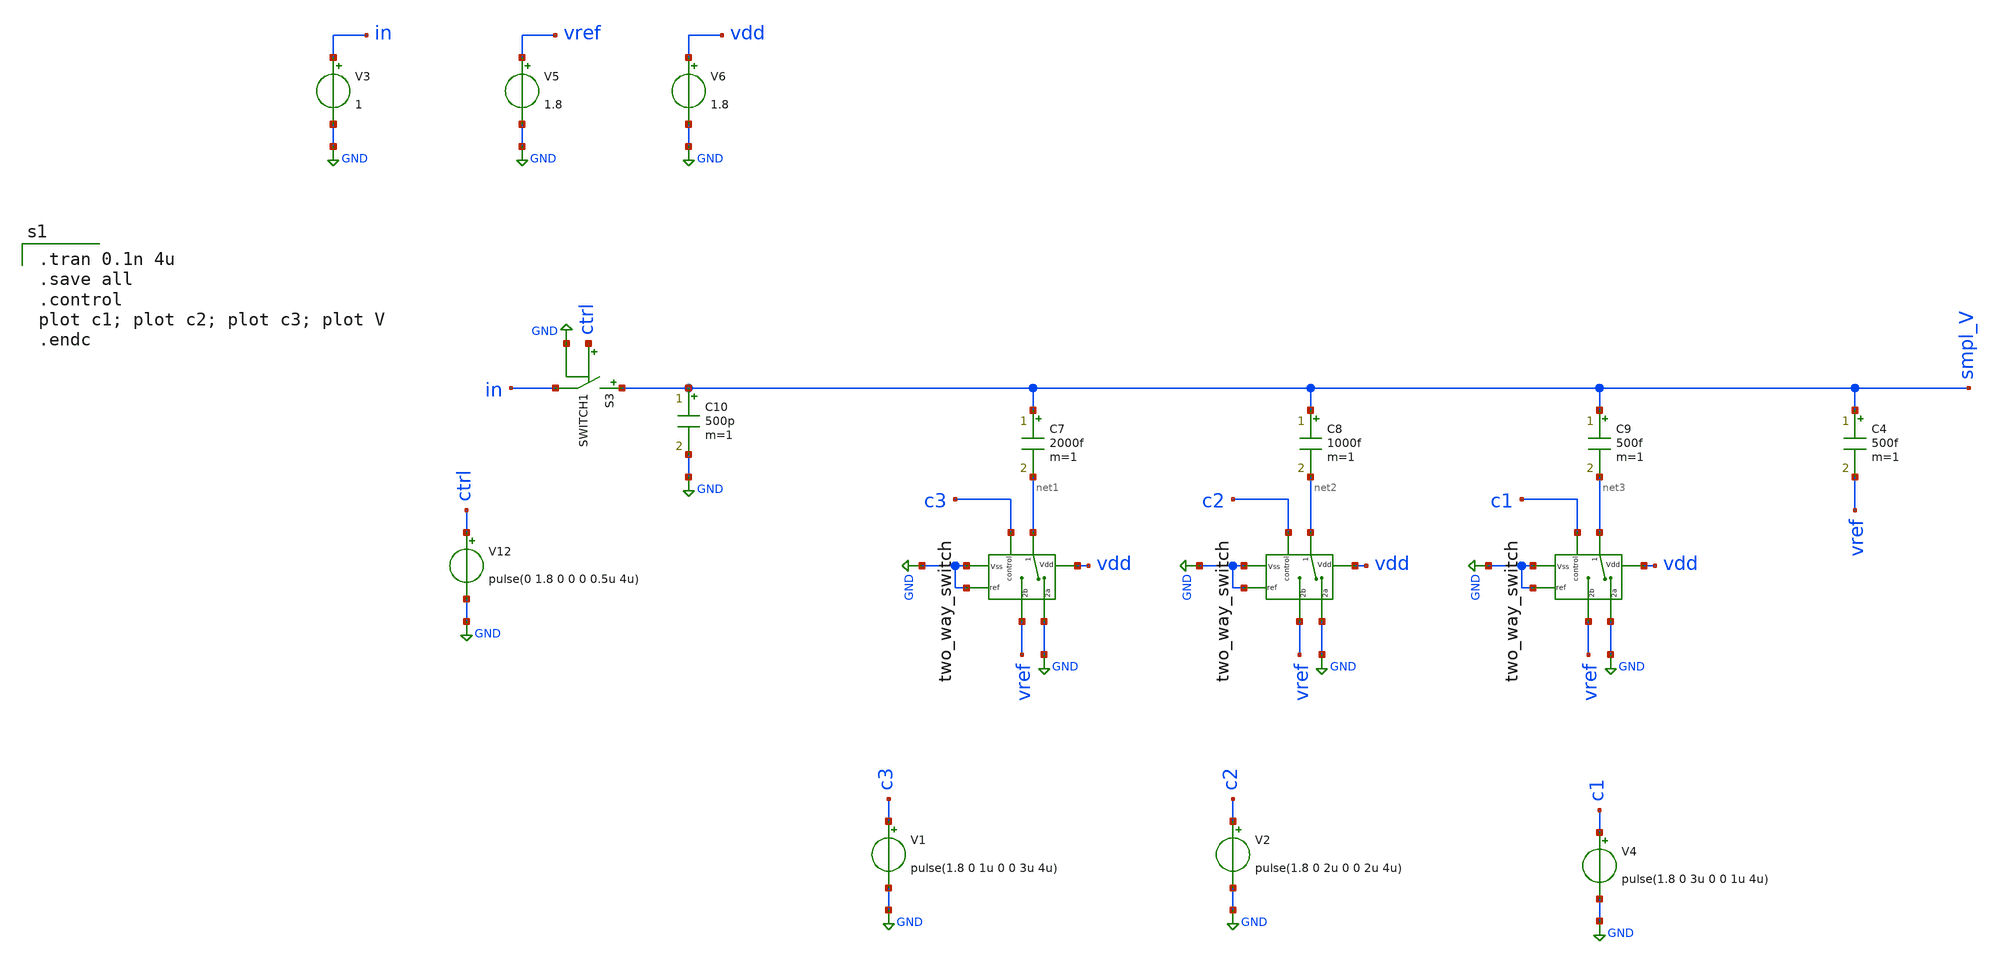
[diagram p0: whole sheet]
** sch_path: Behavioral_model/diff_mode_behavioral.sch
**.subckt diff_mode_behavioral
S3 smpl_V in ctrl GND SWITCH1
C10 smpl_V GND 500p m=1
V12 ctrl GND pulse(0 1.8 0 0 0 0.5u 4u)
V3 in GND 1
C4 smpl_V vref 500f m=1
C7 smpl_V net1 2000f m=1
x7 net1 vdd c3 GND GND vref GND two_way_switch
C8 smpl_V net2 1000f m=1
C9 smpl_V net3 500f m=1
x1 net2 vdd c2 GND GND vref GND two_way_switch
x2 net3 vdd c1 GND GND vref GND two_way_switch
V1 c3 GND pulse(1.8 0 1u 0 0 3u 4u)
V2 c2 GND pulse(1.8 0 2u 0 0 2u 4u)
V4 c1 GND pulse(1.8 0 3u 0 0 1u 4u)
V5 vref GND 1.8
V6 vdd GND 1.8
**** begin user architecture code

.tran 0.1n 4u
.save all
.control
plot c1; plot c2; plot c3; plot V
.endc


.lib /usr/local/share/pdk/sky130A/libs.tech/ngspice/sky130.lib.spice tt


.model switch1 sw vt=0.1 vh=0 ron=1m roff=100G

**** end user architecture code
**.ends

* expanding   symbol:  two_way_switch.sym # of pins=7
** sym_path: Behavioral_model/two_way_switch.sym
** sch_path: Behavioral_model/two_way_switch.sch
.subckt two_way_switch 1 Vdd control ref 2a 2b Vss
*.iopin 2b
*.iopin 2a
*.ipin ref
*.iopin 1
*.ipin Vdd
*.ipin Vss
*.ipin control
S1 1 2a control ref SWITCH1
S2 1 2b net1 ref SWITCH1
x1 Vdd control net1 Vss CMOS_inverter
.ends


* expanding   symbol:  CMOS_inverter.sym # of pins=4
** sym_path: Behavioral_model/CMOS_inverter.sym
** sch_path: Behavioral_model/CMOS_inverter.sch
.subckt CMOS_inverter Vdd Q Q_N Vss
*.ipin Q
*.ipin Vdd
*.ipin Vss
*.opin Q_N
XM1 Q_N Q Vss Vss sky130_fd_pr__nfet_01v8 L=0.15 W=1 nf=1 ad='int((nf+1)/2) * W/nf * 0.29' as='int((nf+2)/2) * W/nf * 0.29'
+ pd='2*int((nf+1)/2) * (W/nf + 0.29)' ps='2*int((nf+2)/2) * (W/nf + 0.29)' nrd='0.29 / W' nrs='0.29 / W'
+ sa=0 sb=0 sd=0 mult=1 m=1
XM3 Q_N Q Vdd Vdd sky130_fd_pr__pfet_01v8 L=0.15 W=1 nf=1 ad='int((nf+1)/2) * W/nf * 0.29' as='int((nf+2)/2) * W/nf * 0.29'
+ pd='2*int((nf+1)/2) * (W/nf + 0.29)' ps='2*int((nf+2)/2) * (W/nf + 0.29)' nrd='0.29 / W' nrs='0.29 / W'
+ sa=0 sb=0 sd=0 mult=1 m=1
.ends

.GLOBAL GND
.end
